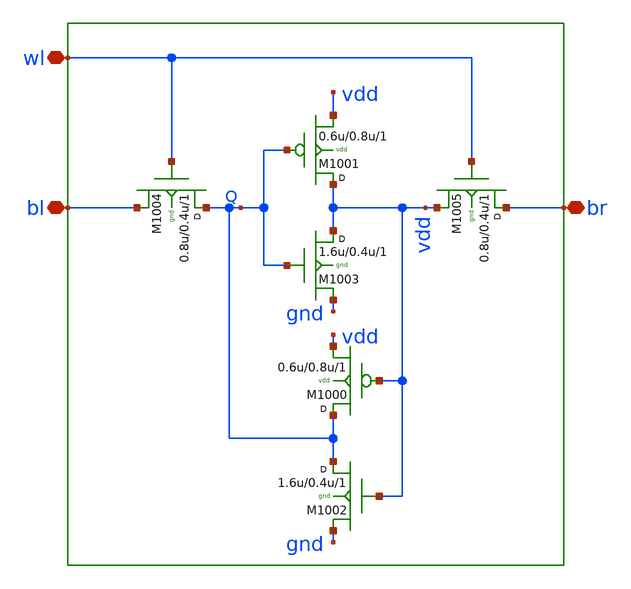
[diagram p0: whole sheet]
** sch_path: sram_4_16_scn4m/replica_cell_1rw.sch
**.subckt replica_cell_1rw bl br wl
*.iopin bl
*.iopin br
*.iopin wl
M1004 Q wl bl gnd n w=0.8u l=0.4u m=1
M1001 vdd Q vdd vdd p w=0.6u l=0.8u m=1
M1003 vdd Q gnd gnd n w=1.6u l=0.4u m=1
M1002 Q vdd gnd gnd n w=1.6u l=0.4u m=1
M1000 Q vdd vdd vdd p w=0.6u l=0.8u m=1
M1005 br wl vdd gnd n w=0.8u l=0.4u m=1
**.ends
.end
